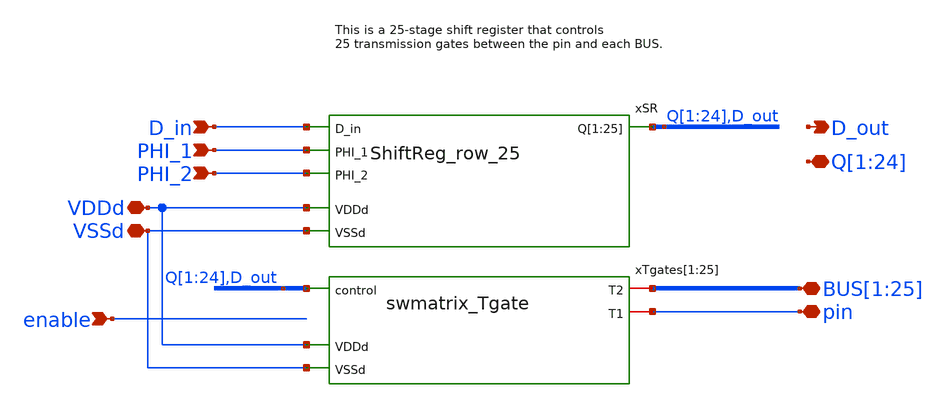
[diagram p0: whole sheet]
** sch_path: swmatrix_row_25/swmatrix_row_25.sch
**.subckt swmatrix_row_25 pin PHI_2 PHI_1
*+ BUS[1],BUS[2],BUS[3],BUS[4],BUS[5],BUS[6],BUS[7],BUS[8],BUS[9],BUS[10],BUS[11],BUS[12],BUS[13],BUS[14],BUS[15],BUS[16],BUS[17],BUS[18],BUS[19],BUS[20],BUS[21],BUS[22],BUS[23],BUS[24],BUS[25] D_in
*+ Q[1],Q[2],Q[3],Q[4],Q[5],Q[6],Q[7],Q[8],Q[9],Q[10],Q[11],Q[12],Q[13],Q[14],Q[15],Q[16],Q[17],Q[18],Q[19],Q[20],Q[21],Q[22],Q[23],Q[24] VDDd VSSd enable D_out
*.iopin pin
*.ipin PHI_2
*.ipin PHI_1
*.iopin
*+ BUS[1],BUS[2],BUS[3],BUS[4],BUS[5],BUS[6],BUS[7],BUS[8],BUS[9],BUS[10],BUS[11],BUS[12],BUS[13],BUS[14],BUS[15],BUS[16],BUS[17],BUS[18],BUS[19],BUS[20],BUS[21],BUS[22],BUS[23],BUS[24],BUS[25]
*.ipin D_in
*.iopin
*+ Q[1],Q[2],Q[3],Q[4],Q[5],Q[6],Q[7],Q[8],Q[9],Q[10],Q[11],Q[12],Q[13],Q[14],Q[15],Q[16],Q[17],Q[18],Q[19],Q[20],Q[21],Q[22],Q[23],Q[24]
*.iopin VDDd
*.iopin VSSd
*.ipin enable
*.opin D_out
xSR Q[1] Q[2] Q[3] Q[4] Q[5] Q[6] Q[7] Q[8] Q[9] Q[10] Q[11] Q[12] Q[13] Q[14] Q[15] Q[16] Q[17]
+ Q[18] Q[19] Q[20] Q[21] Q[22] Q[23] Q[24] D_out D_in PHI_1 PHI_2 VDDd VSSd ShiftReg_row_25
xTgates[1] Q[1] BUS[1] pin VDDd VSSd swmatrix_Tgate
xTgates[2] Q[2] BUS[2] pin VDDd VSSd swmatrix_Tgate
xTgates[3] Q[3] BUS[3] pin VDDd VSSd swmatrix_Tgate
xTgates[4] Q[4] BUS[4] pin VDDd VSSd swmatrix_Tgate
xTgates[5] Q[5] BUS[5] pin VDDd VSSd swmatrix_Tgate
xTgates[6] Q[6] BUS[6] pin VDDd VSSd swmatrix_Tgate
xTgates[7] Q[7] BUS[7] pin VDDd VSSd swmatrix_Tgate
xTgates[8] Q[8] BUS[8] pin VDDd VSSd swmatrix_Tgate
xTgates[9] Q[9] BUS[9] pin VDDd VSSd swmatrix_Tgate
xTgates[10] Q[10] BUS[10] pin VDDd VSSd swmatrix_Tgate
xTgates[11] Q[11] BUS[11] pin VDDd VSSd swmatrix_Tgate
xTgates[12] Q[12] BUS[12] pin VDDd VSSd swmatrix_Tgate
xTgates[13] Q[13] BUS[13] pin VDDd VSSd swmatrix_Tgate
xTgates[14] Q[14] BUS[14] pin VDDd VSSd swmatrix_Tgate
xTgates[15] Q[15] BUS[15] pin VDDd VSSd swmatrix_Tgate
xTgates[16] Q[16] BUS[16] pin VDDd VSSd swmatrix_Tgate
xTgates[17] Q[17] BUS[17] pin VDDd VSSd swmatrix_Tgate
xTgates[18] Q[18] BUS[18] pin VDDd VSSd swmatrix_Tgate
xTgates[19] Q[19] BUS[19] pin VDDd VSSd swmatrix_Tgate
xTgates[20] Q[20] BUS[20] pin VDDd VSSd swmatrix_Tgate
xTgates[21] Q[21] BUS[21] pin VDDd VSSd swmatrix_Tgate
xTgates[22] Q[22] BUS[22] pin VDDd VSSd swmatrix_Tgate
xTgates[23] Q[23] BUS[23] pin VDDd VSSd swmatrix_Tgate
xTgates[24] Q[24] BUS[24] pin VDDd VSSd swmatrix_Tgate
xTgates[25] D_out BUS[25] pin VDDd VSSd swmatrix_Tgate
**.ends
.end
